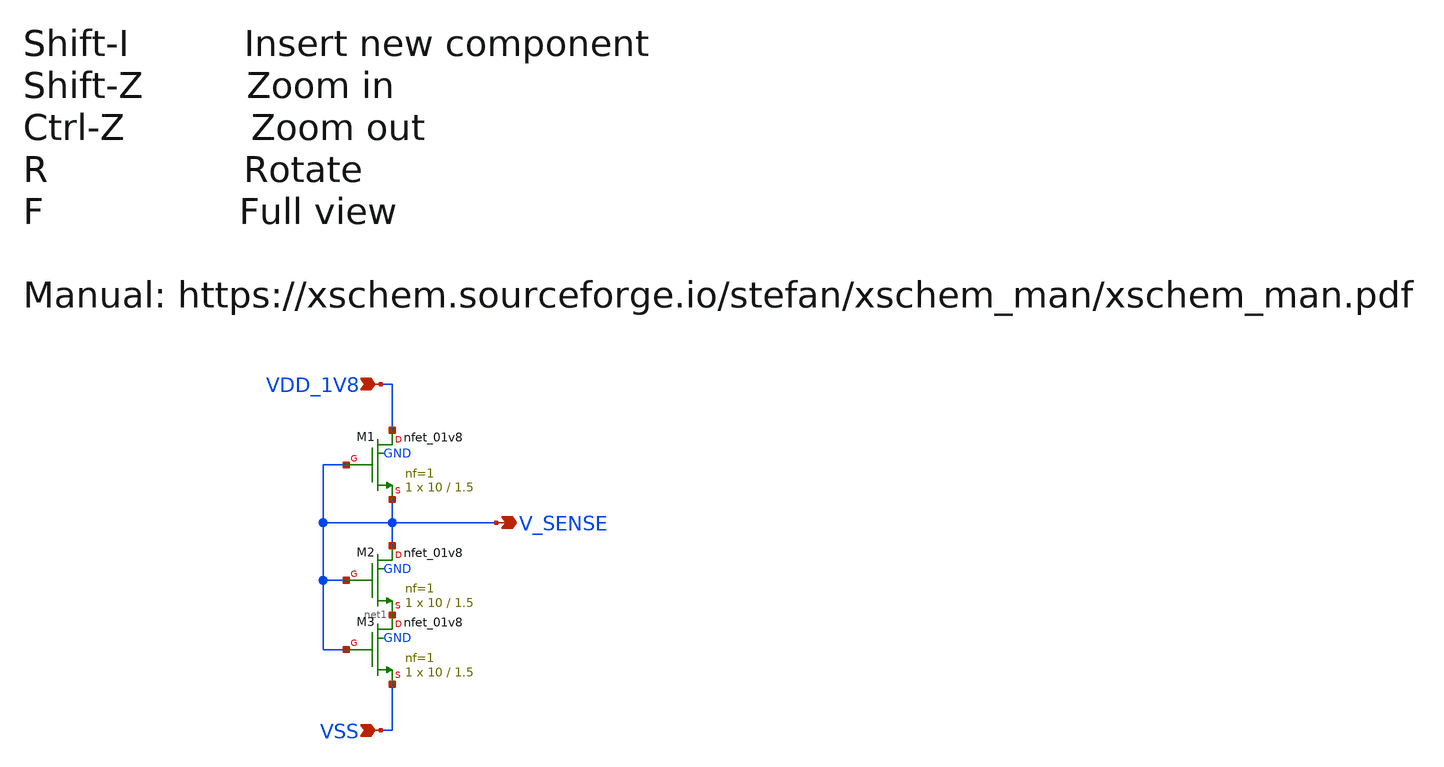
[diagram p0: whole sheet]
** sch_path: design/RPLY_TEMP_SENS_SKY130NM/TEMP_SENS_ELEMENT_2.sch
**.subckt TEMP_SENS_ELEMENT_2 VDD_1V8 V_SENSE VSS
*.ipin VDD_1V8
*.opin V_SENSE
*.ipin VSS
XM1 VDD_1V8 V_SENSE V_SENSE GND sky130_fd_pr__nfet_01v8 L=1.5 W=10 nf=1 ad='int((nf+1)/2) * W/nf * 0.29'
+ as='int((nf+2)/2) * W/nf * 0.29' pd='2*int((nf+1)/2) * (W/nf + 0.29)' ps='2*int((nf+2)/2) * (W/nf + 0.29)'
+ nrd='0.29 / W' nrs='0.29 / W' sa=0 sb=0 sd=0 mult=1 m=1
XM2 V_SENSE V_SENSE net1 GND sky130_fd_pr__nfet_01v8 L=1.5 W=10 nf=1 ad='int((nf+1)/2) * W/nf * 0.29'
+ as='int((nf+2)/2) * W/nf * 0.29' pd='2*int((nf+1)/2) * (W/nf + 0.29)' ps='2*int((nf+2)/2) * (W/nf + 0.29)'
+ nrd='0.29 / W' nrs='0.29 / W' sa=0 sb=0 sd=0 mult=1 m=1
XM3 net1 V_SENSE VSS GND sky130_fd_pr__nfet_01v8 L=1.5 W=10 nf=1 ad='int((nf+1)/2) * W/nf * 0.29' as='int((nf+2)/2) * W/nf * 0.29'
+ pd='2*int((nf+1)/2) * (W/nf + 0.29)' ps='2*int((nf+2)/2) * (W/nf + 0.29)' nrd='0.29 / W' nrs='0.29 / W'
+ sa=0 sb=0 sd=0 mult=1 m=1
**.ends
.end
